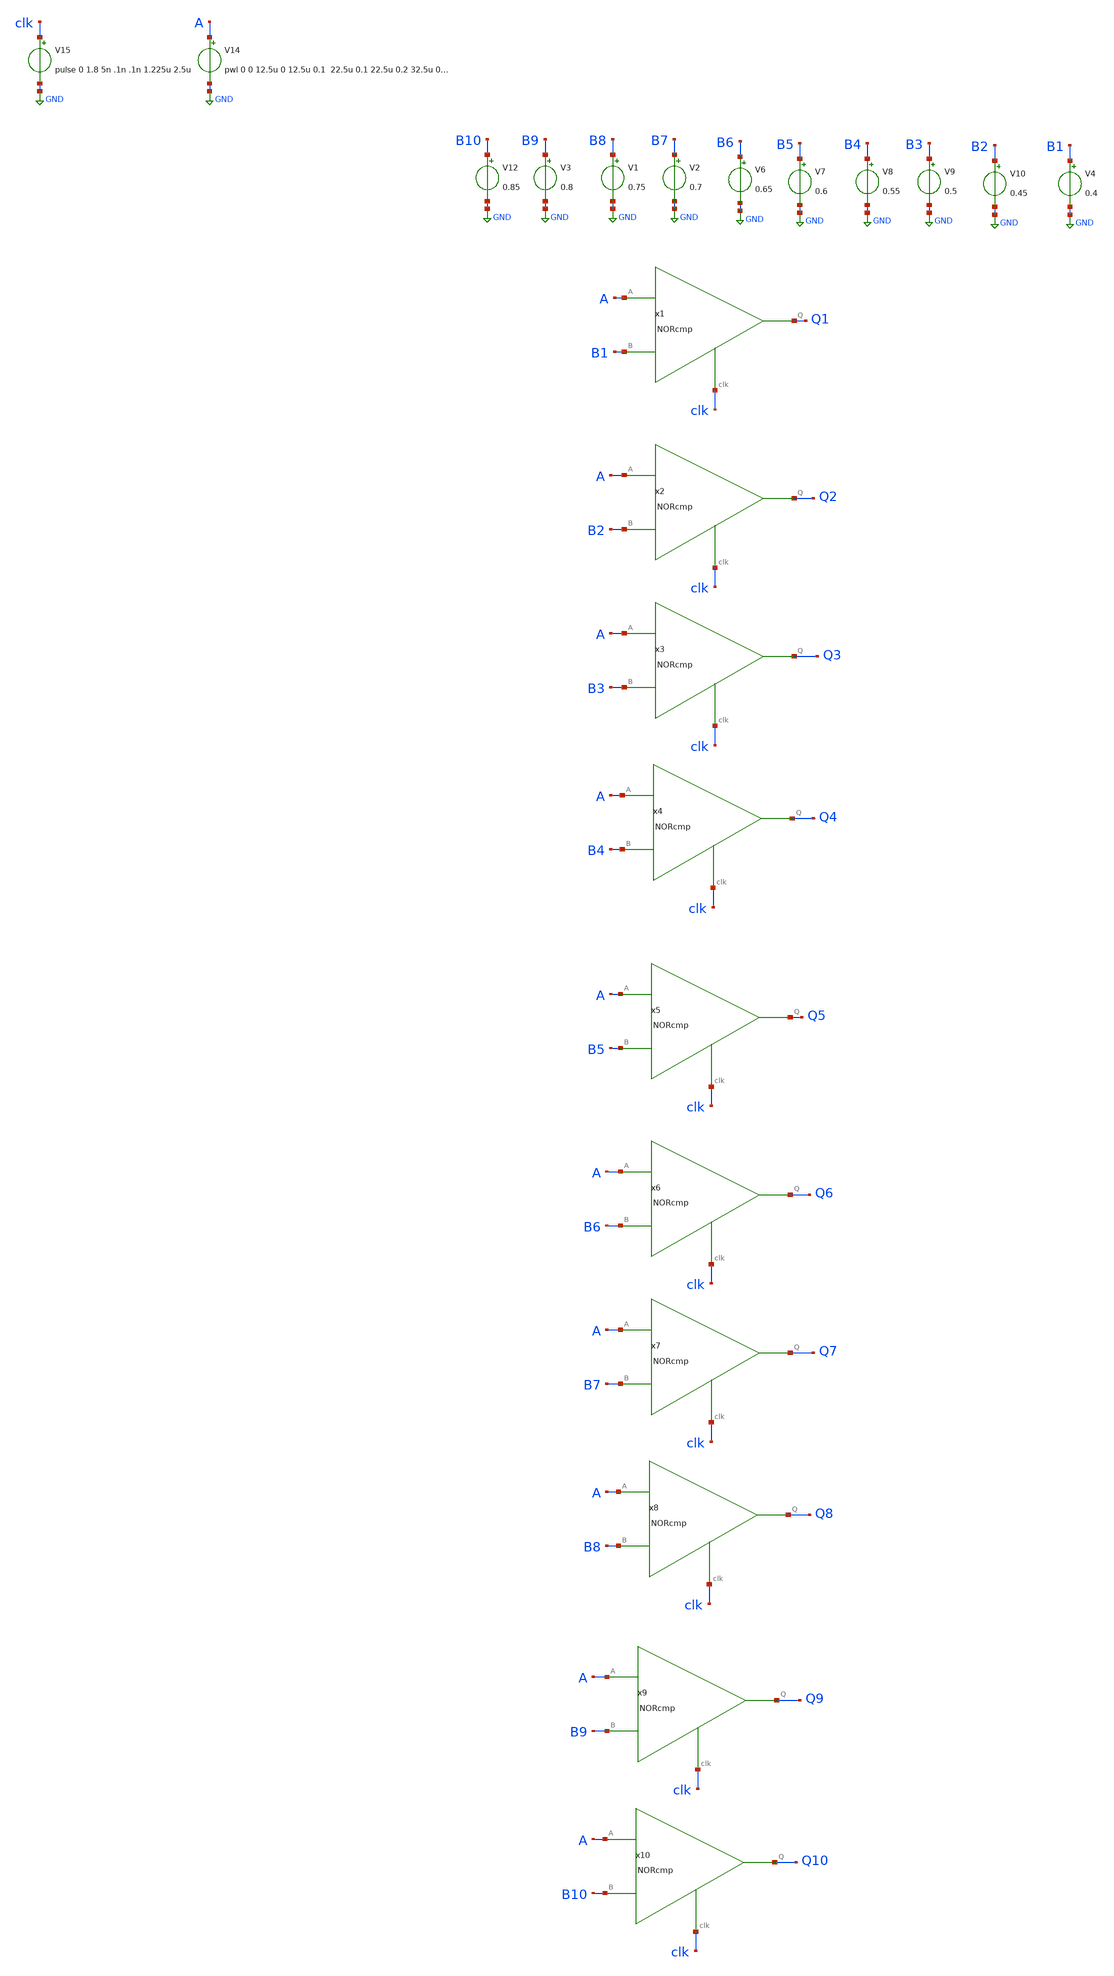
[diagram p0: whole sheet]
** sch_path: cmp/Schematics/cmpNOR_testbench.sch
**.subckt cmpNOR_testbench
V3 B9 GND 0.8
V1 B8 GND 0.75
V2 B7 GND 0.7
V6 B6 GND 0.65
V7 B5 GND 0.6
V8 B4 GND 0.55
V9 B3 GND 0.5
V10 B2 GND 0.45
x1 A clk B1 Q1 NORcmp
x2 A clk B2 Q2 NORcmp
x3 A clk B3 Q3 NORcmp
x4 A clk B4 Q4 NORcmp
x5 A clk B5 Q5 NORcmp
x6 A clk B6 Q6 NORcmp
x7 A clk B7 Q7 NORcmp
x8 A clk B8 Q8 NORcmp
V12 B10 GND 0.85
V14 A GND pwl 0 0 12.5u 0 12.5u 0.1 22.5u 0.1 22.5u 0.2 32.5u 0.2 32.5u 0.3 42.5u 0.3 42.5u 0.4
+ 52.5u 0.4 52.5u 0.5 62.5u 0.5 62.5u 0.6 72.5u 0.6 72.5u 0.7 82.5u 0.7 82.5u 0.8 92.5u 0.8 92.5u 0.9
V15 clk GND pulse 0 1.8 5n .1n .1n 1.225u 2.5u
x9 A clk B9 Q9 NORcmp
x10 A clk B10 Q10 NORcmp
V4 B1 GND 0.4
**** begin user architecture code

.include $::SKYWATER_MODELS/cells/nfet_01v8/sky130_fd_pr__nfet_01v8__tt.corner.spice
.include $::SKYWATER_MODELS/cells/nfet_01v8_lvt/sky130_fd_pr__nfet_01v8_lvt__tt.corner.spice
.include $::SKYWATER_MODELS/cells/pfet_01v8/sky130_fd_pr__pfet_01v8__tt.corner.spice
.include $::SKYWATER_MODELS/cells/nfet_03v3_nvt/sky130_fd_pr__nfet_03v3_nvt__tt.corner.spice
.include $::SKYWATER_MODELS/cells/nfet_05v0_nvt/sky130_fd_pr__nfet_05v0_nvt__tt.corner.spice
.include $::SKYWATER_MODELS/cells/esd_nfet_01v8/sky130_fd_pr__esd_nfet_01v8__tt.corner.spice
.include $::SKYWATER_MODELS/cells/pfet_01v8_lvt/sky130_fd_pr__pfet_01v8_lvt__tt.corner.spice
.include $::SKYWATER_MODELS/cells/pfet_01v8_hvt/sky130_fd_pr__pfet_01v8_hvt__tt.corner.spice
.include $::SKYWATER_MODELS/cells/esd_pfet_g5v0d10v5/sky130_fd_pr__esd_pfet_g5v0d10v5__tt.corner.spice
.include $::SKYWATER_MODELS/cells/pfet_g5v0d10v5/sky130_fd_pr__pfet_g5v0d10v5__tt.corner.spice
.include $::SKYWATER_MODELS/cells/pfet_g5v0d16v0/sky130_fd_pr__pfet_g5v0d16v0__tt.corner.spice
.include $::SKYWATER_MODELS/cells/nfet_g5v0d10v5/sky130_fd_pr__nfet_g5v0d10v5__tt.corner.spice
.include $::SKYWATER_MODELS/cells/nfet_g5v0d16v0/sky130_fd_pr__nfet_g5v0d16v0__tt_discrete.corner.spice
.include $::SKYWATER_MODELS/cells/esd_nfet_g5v0d10v5/sky130_fd_pr__esd_nfet_g5v0d10v5__tt.corner.spice
.include $::SKYWATER_MODELS/models/corners/tt/nonfet.spice
* Mismatch parameters
.include $::SKYWATER_MODELS/cells/nfet_01v8/sky130_fd_pr__nfet_01v8__mismatch.corner.spice
.include $::SKYWATER_MODELS/cells/pfet_01v8/sky130_fd_pr__pfet_01v8__mismatch.corner.spice
.include $::SKYWATER_MODELS/cells/nfet_01v8_lvt/sky130_fd_pr__nfet_01v8_lvt__mismatch.corner.spice
.include $::SKYWATER_MODELS/cells/pfet_01v8_lvt/sky130_fd_pr__pfet_01v8_lvt__mismatch.corner.spice
.include $::SKYWATER_MODELS/cells/pfet_01v8_hvt/sky130_fd_pr__pfet_01v8_hvt__mismatch.corner.spice
.include $::SKYWATER_MODELS/cells/nfet_g5v0d10v5/sky130_fd_pr__nfet_g5v0d10v5__mismatch.corner.spice
.include $::SKYWATER_MODELS/cells/pfet_g5v0d10v5/sky130_fd_pr__pfet_g5v0d10v5__mismatch.corner.spice
.include $::SKYWATER_MODELS/cells/nfet_05v0_nvt/sky130_fd_pr__nfet_05v0_nvt__mismatch.corner.spice
.include $::SKYWATER_MODELS/cells/nfet_03v3_nvt/sky130_fd_pr__nfet_03v3_nvt__mismatch.corner.spice
* Resistor$::SKYWATER_MODELS/Capacitor
.include $::SKYWATER_MODELS/models/r+c/res_typical__cap_typical.spice
.include $::SKYWATER_MODELS/models/r+c/res_typical__cap_typical__lin.spice
* Special cells
.include $::SKYWATER_MODELS/models/corners/tt/specialized_cells.spice
* All models
.include $::SKYWATER_MODELS/models/all.spice
* Corner
.include $::SKYWATER_MODELS/models/corners/tt/rf.spice
.include ~/skywater-pdk/libraries/sky130_fd_sc_hd/latest/cells/nand2/sky130_fd_sc_hd__nand2_1.spice
.include ~/skywater-pdk/libraries/sky130_fd_sc_hd/latest/cells/nor3/sky130_fd_sc_hd__nor3_1.spice
.include ~/skywater-pdk/libraries/sky130_fd_sc_hd/latest/cells/dfrtp/sky130_fd_sc_hd__dfrtp_1.spice
.include ~/skywater-pdk/libraries/sky130_fd_sc_hd/latest/cells/nor2/sky130_fd_sc_hd__nor2_1.spice
.include ~/skywater-pdk/libraries/sky130_fd_sc_hd/latest/cells/dlrbn/sky130_fd_sc_hd__dlrbn_1.spice
.include ~/skywater-pdk/libraries/sky130_fd_sc_hd/latest/cells/a31o/sky130_fd_sc_hd__a31o_2.spice
.include ~/skywater-pdk/libraries/sky130_fd_sc_hd/latest/cells/inv/sky130_fd_sc_hd__inv_1.spice

**** end user architecture code
**.ends
.GLOBAL GND
**** begin user architecture code


.temp 25
vvcc vcc 0 1.8
vvss vss 0 0
.control
tran 1u 100u
plot A CLK+2 Q1+4 Q2+6 Q3+8 Q4+10 Q5+12 Q6+14 Q7+16 Q8+18 Q9+20 Q10+22
.endc


**** end user architecture code
.end
